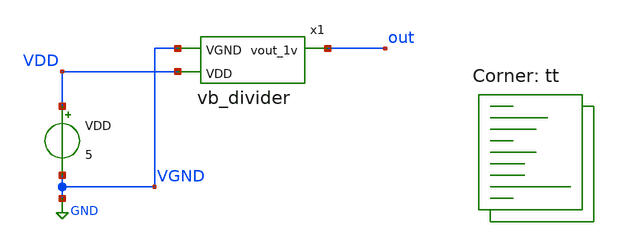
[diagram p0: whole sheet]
** sch_path: xschem/test_vb_divider.sch
**.subckt test_vb_divider
x1 VDD GND out vb_divider
VDD VDD GND 5
**** begin user architecture code
.lib $::SKYWATER_MODELS/sky130.lib.spice tt



.include 'vb_divider.spice'
* .options reltol=0.0001 abstol=10e-15
.options savecurrents
.control
  save all
  op
  remzerovec
  write test_vb_divider.raw
  set appendwrite
  * dc sweep
  dc VDD 4.5 5.5 0.1
  remzerovec
  write test_vb_divider.raw
  * tran
  tran 100p 300n
  remzerovec
  write test_vb_divider.raw
.endc



**** end user architecture code
**.ends
.GLOBAL GND
.end
